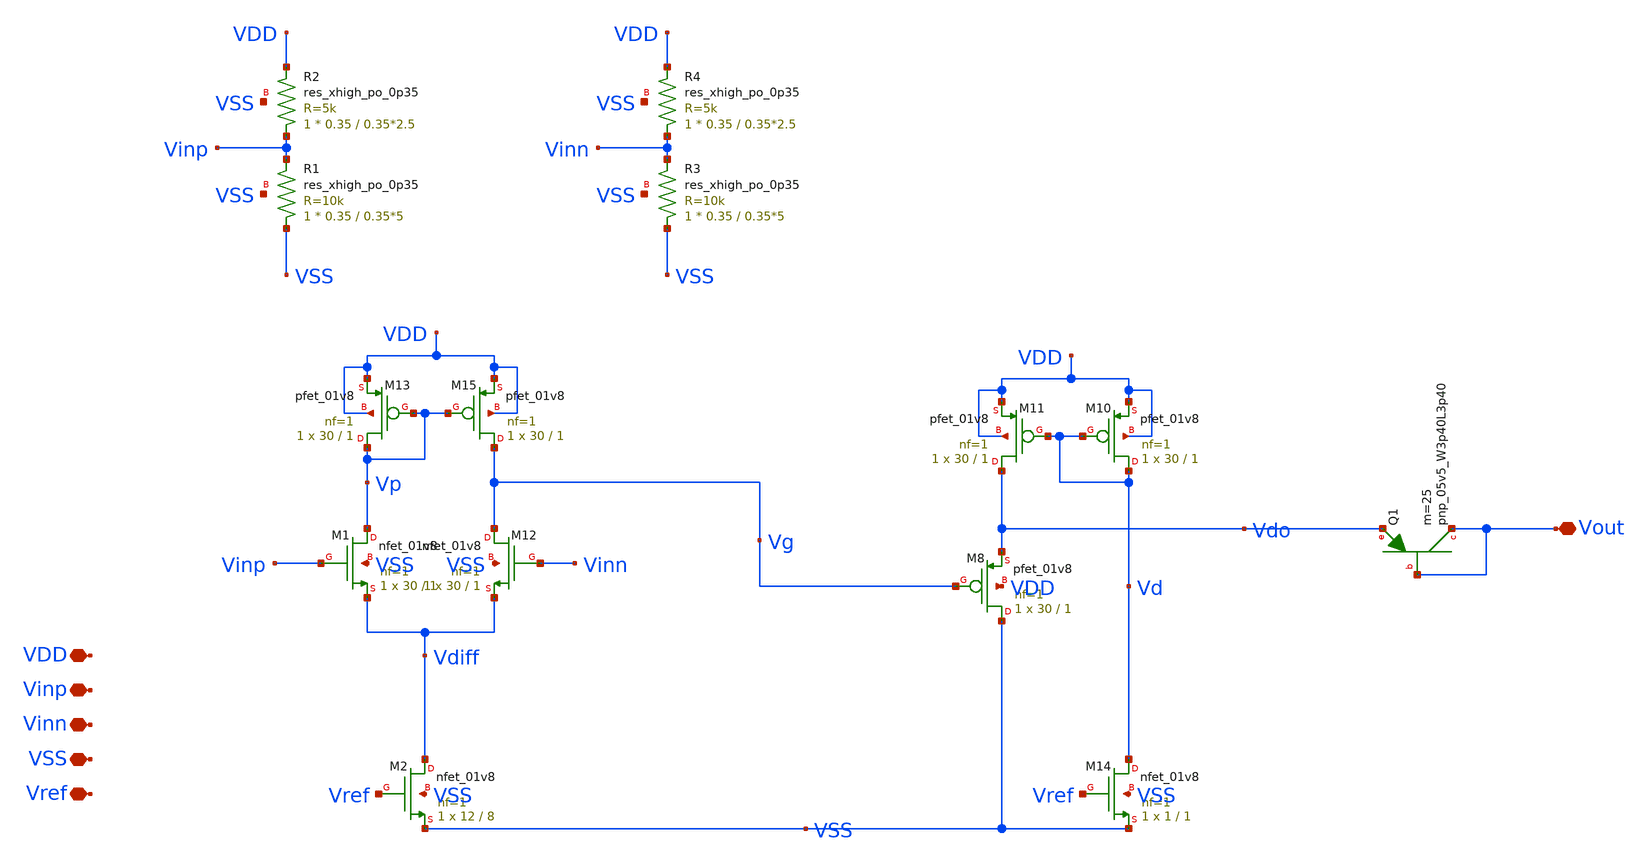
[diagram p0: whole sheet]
** sch_path: hw08/xschem/demod.sch
**.subckt demod Vref VSS Vinn Vinp VDD Vout
*.iopin Vref
*.iopin VSS
*.iopin Vinn
*.iopin Vinp
*.iopin VDD
*.iopin Vout
XM1 Vp Vinp Vdiff VSS sky130_fd_pr__nfet_01v8 L=1 W=30 nf=1 ad='int((nf+1)/2) * W/nf * 0.29' as='int((nf+2)/2) * W/nf * 0.29'
+ pd='2*int((nf+1)/2) * (W/nf + 0.29)' ps='2*int((nf+2)/2) * (W/nf + 0.29)' nrd='0.29 / W' nrs='0.29 / W'
+ sa=0 sb=0 sd=0 mult=1 m=1
XM12 Vg Vinn Vdiff VSS sky130_fd_pr__nfet_01v8 L=1 W=30 nf=1 ad='int((nf+1)/2) * W/nf * 0.29' as='int((nf+2)/2) * W/nf * 0.29'
+ pd='2*int((nf+1)/2) * (W/nf + 0.29)' ps='2*int((nf+2)/2) * (W/nf + 0.29)' nrd='0.29 / W' nrs='0.29 / W'
+ sa=0 sb=0 sd=0 mult=1 m=1
XM15 Vg Vp VDD VDD sky130_fd_pr__pfet_01v8 L=1 W=30 nf=1 ad='int((nf+1)/2) * W/nf * 0.29' as='int((nf+2)/2) * W/nf * 0.29'
+ pd='2*int((nf+1)/2) * (W/nf + 0.29)' ps='2*int((nf+2)/2) * (W/nf + 0.29)' nrd='0.29 / W' nrs='0.29 / W'
+ sa=0 sb=0 sd=0 mult=1 m=1
XM13 Vp Vp VDD VDD sky130_fd_pr__pfet_01v8 L=1 W=30 nf=1 ad='int((nf+1)/2) * W/nf * 0.29' as='int((nf+2)/2) * W/nf * 0.29'
+ pd='2*int((nf+1)/2) * (W/nf + 0.29)' ps='2*int((nf+2)/2) * (W/nf + 0.29)' nrd='0.29 / W' nrs='0.29 / W'
+ sa=0 sb=0 sd=0 mult=1 m=1
XM2 Vdiff Vref VSS VSS sky130_fd_pr__nfet_01v8 L=8 W=12 nf=1 ad='int((nf+1)/2) * W/nf * 0.29' as='int((nf+2)/2) * W/nf * 0.29'
+ pd='2*int((nf+1)/2) * (W/nf + 0.29)' ps='2*int((nf+2)/2) * (W/nf + 0.29)' nrd='0.29 / W' nrs='0.29 / W'
+ sa=0 sb=0 sd=0 mult=1 m=1
XM10 Vd Vd VDD VDD sky130_fd_pr__pfet_01v8 L=1 W=30 nf=1 ad='int((nf+1)/2) * W/nf * 0.29' as='int((nf+2)/2) * W/nf * 0.29'
+ pd='2*int((nf+1)/2) * (W/nf + 0.29)' ps='2*int((nf+2)/2) * (W/nf + 0.29)' nrd='0.29 / W' nrs='0.29 / W'
+ sa=0 sb=0 sd=0 mult=1 m=1
XM11 Vdo Vd VDD VDD sky130_fd_pr__pfet_01v8 L=1 W=30 nf=1 ad='int((nf+1)/2) * W/nf * 0.29' as='int((nf+2)/2) * W/nf * 0.29'
+ pd='2*int((nf+1)/2) * (W/nf + 0.29)' ps='2*int((nf+2)/2) * (W/nf + 0.29)' nrd='0.29 / W' nrs='0.29 / W'
+ sa=0 sb=0 sd=0 mult=1 m=1
XM14 Vd Vref VSS VSS sky130_fd_pr__nfet_01v8 L=1 W=1 nf=1 ad='int((nf+1)/2) * W/nf * 0.29' as='int((nf+2)/2) * W/nf * 0.29'
+ pd='2*int((nf+1)/2) * (W/nf + 0.29)' ps='2*int((nf+2)/2) * (W/nf + 0.29)' nrd='0.29 / W' nrs='0.29 / W'
+ sa=0 sb=0 sd=0 mult=1 m=1
XM8 VSS Vg Vdo VDD sky130_fd_pr__pfet_01v8 L=1 W=30 nf=1 ad='int((nf+1)/2) * W/nf * 0.29' as='int((nf+2)/2) * W/nf * 0.29'
+ pd='2*int((nf+1)/2) * (W/nf + 0.29)' ps='2*int((nf+2)/2) * (W/nf + 0.29)' nrd='0.29 / W' nrs='0.29 / W'
+ sa=0 sb=0 sd=0 mult=1 m=1
XQ1 Vout Vout Vdo sky130_fd_pr__pnp_05v5_W3p40L3p40 m=25
XR1 VSS Vinp VSS sky130_fd_pr__res_xhigh_po_0p35 L=0.35*5 mult=1 m=1
XR2 Vinp VDD VSS sky130_fd_pr__res_xhigh_po_0p35 L=0.35*2.5 mult=1 m=1
XR3 VSS Vinn VSS sky130_fd_pr__res_xhigh_po_0p35 L=0.35*5 mult=1 m=1
XR4 Vinn VDD VSS sky130_fd_pr__res_xhigh_po_0p35 L=0.35*2.5 mult=1 m=1
**.ends
.end
